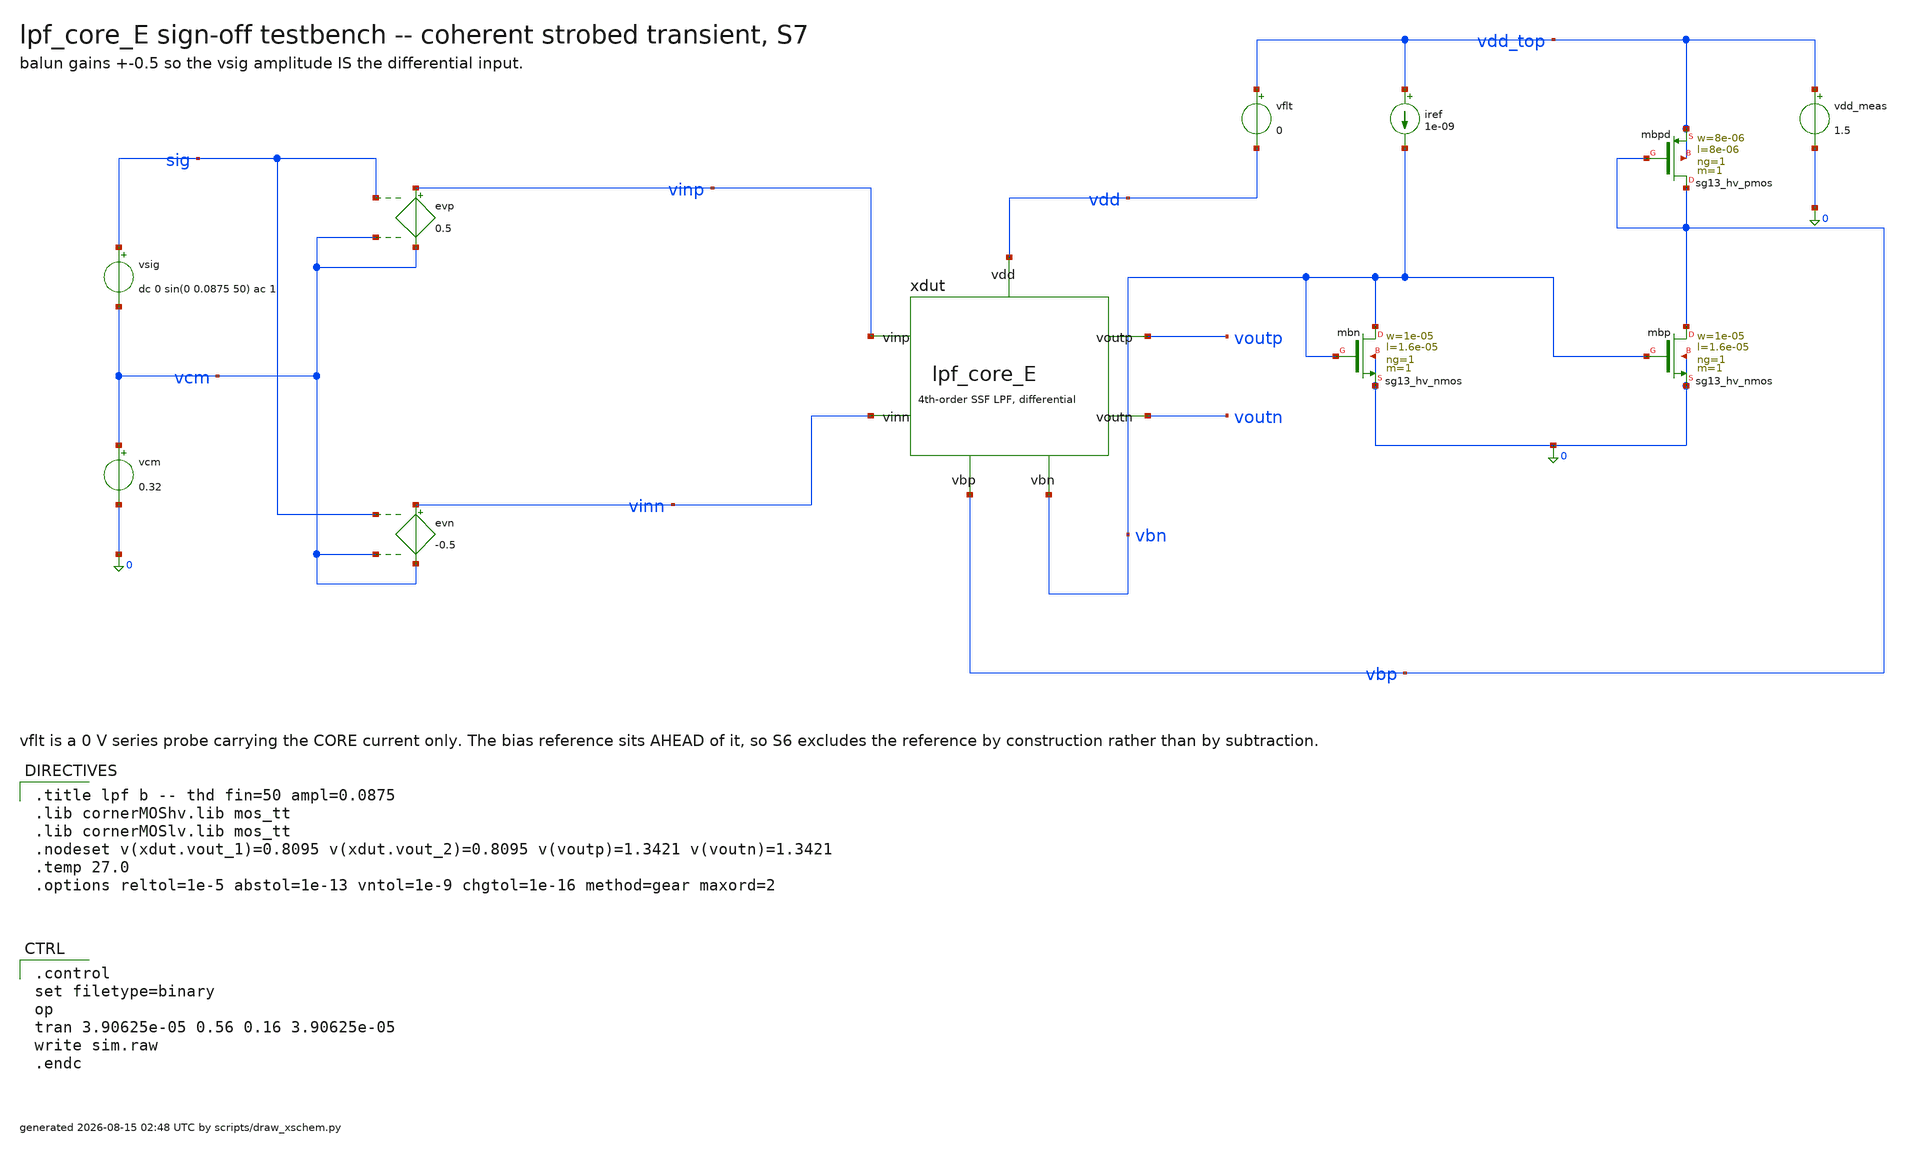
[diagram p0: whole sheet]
** sch_path: signoff/pre-pvt/E-combo/lpf_tb_E_thd.sch
**.subckt lpf_tb_E_thd
vsig sig vcm dc 0 sin(0 0.0875 50) ac 1
vcm vcm 0 0.32
evp vinp vcm sig vcm 0.5
evn vinn vcm sig vcm -0.5
xdut vinp vinn voutp voutn vbn vbp vdd lpf_core_E
vflt vdd_top vdd 0
vdd_meas vdd_top 0 1.5
iref vdd_top vbn 1e-09
Xmbn vbn vbn 0 0 sg13_hv_nmos w=1e-05 l=1.6e-05 ng=1 m=1 mm_ok=1
Xmbp vbp vbn 0 0 sg13_hv_nmos w=1e-05 l=1.6e-05 ng=1 m=1 mm_ok=1
Xmbpd vbp vbp vdd_top vdd_top sg13_hv_pmos w=8e-06 l=8e-06 ng=1 m=1 mm_ok=1
**** begin user architecture code

.title lpf b -- thd fin=50 ampl=0.0875
.lib cornerMOShv.lib mos_tt
.lib cornerMOSlv.lib mos_tt
.nodeset v(xdut.vout_1)=0.8095 v(xdut.vout_2)=0.8095 v(voutp)=1.3421 v(voutn)=1.3421
.temp 27.0
.options reltol=1e-5 abstol=1e-13 vntol=1e-9 chgtol=1e-16 method=gear maxord=2


.control
set filetype=binary
op
tran 3.90625e-05 0.56 0.16 3.90625e-05
write sim.raw
.endc

**** end user architecture code
**.ends

* expanding   symbol:  lpf_core_E.sym # of pins=7
** sym_path: signoff/E-combo/lpf_core_E.sym
** sch_path: signoff/E-combo/lpf_core_E.sch
.subckt lpf_core_E vinp vinn voutp voutn vbn vbp vdd
*.ipin vinp
*.ipin vinn
*.opin voutp
*.opin voutn
*.ipin vdd
*.ipin vbn
*.ipin vbp
Xm2 net2 vinp vout_1 vout_1 sg13_hv_pmos w=8e-06 l=8e-06 ng=1 m=1 mm_ok=1
Xm5 net3 vinn vout_2 vout_2 sg13_hv_pmos w=8e-06 l=8e-06 ng=1 m=1 mm_ok=1
Xm4 vout_1 net2 0 0 sg13_hv_nmos w=1e-06 l=4.5e-05 ng=1 m=1 mm_ok=1
Xm8 vout_2 net3 0 0 sg13_hv_nmos w=1e-06 l=4.5e-05 ng=1 m=1 mm_ok=1
Xm9 net2 vbn 0 0 sg13_hv_nmos w=1e-05 l=1.6e-05 ng=1 m=1 mm_ok=1
Xm10 net3 vbn 0 0 sg13_hv_nmos w=1e-05 l=1.6e-05 ng=1 m=1 mm_ok=1
Xmst vout_1 vbn net4 net4 sg13_hv_pmos w=4.8e-07 l=3.36e-05 ng=1 m=1 mm_ok=1
Xmstn vout_2 vbn net1 net1 sg13_hv_pmos w=4.8e-07 l=3.36e-05 ng=1 m=1 mm_ok=1
Xm0 net4 vout_1 voutp voutp sg13_hv_pmos w=8e-06 l=8e-06 ng=1 m=1 mm_ok=1
Xm1 net1 vout_2 voutn voutn sg13_hv_pmos w=8e-06 l=8e-06 ng=1 m=1 mm_ok=1
Xm14 voutp net4 vdd vdd sg13_lv_pmos w=1.28e-06 l=9.6e-05 ng=1 m=1 mm_ok=1
Xm15 voutn net1 vdd vdd sg13_lv_pmos w=1.28e-06 l=9.6e-05 ng=1 m=1 mm_ok=1
c13 net2 vout_1 8.61884e-12 m=1
c17 net3 vout_2 8.61884e-12 m=1
c19 vout_2 vout_1 2.36443e-11 m=1
c1 voutp net4 8.10786e-11 m=1
c10 voutn net1 8.10786e-11 m=1
c12 voutn voutp 1.69787e-11 m=1
.ends

.end
